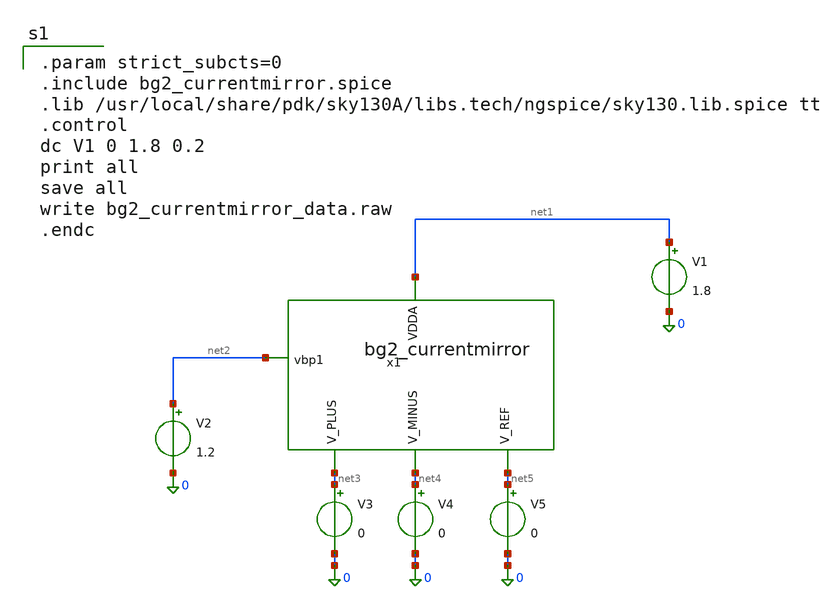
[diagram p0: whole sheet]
** sch_path: lef/bg2_currentmirror_tb.sch
**.subckt bg2_currentmirror_tb
V1 net1 0 1.8
V2 net2 0 1.2
x1 net1 net2 net4 net5 net3 bg2_currentmirror
V3 net3 0 0
V4 net4 0 0
V5 net5 0 0
**** begin user architecture code

.param strict_subcts=0
.include bg2_currentmirror.spice
.lib /usr/local/share/pdk/sky130A/libs.tech/ngspice/sky130.lib.spice tt
.control
dc V1 0 1.8 0.2
print all
save all
write bg2_currentmirror_data.raw
.endc

**** end user architecture code
**.ends
.end
